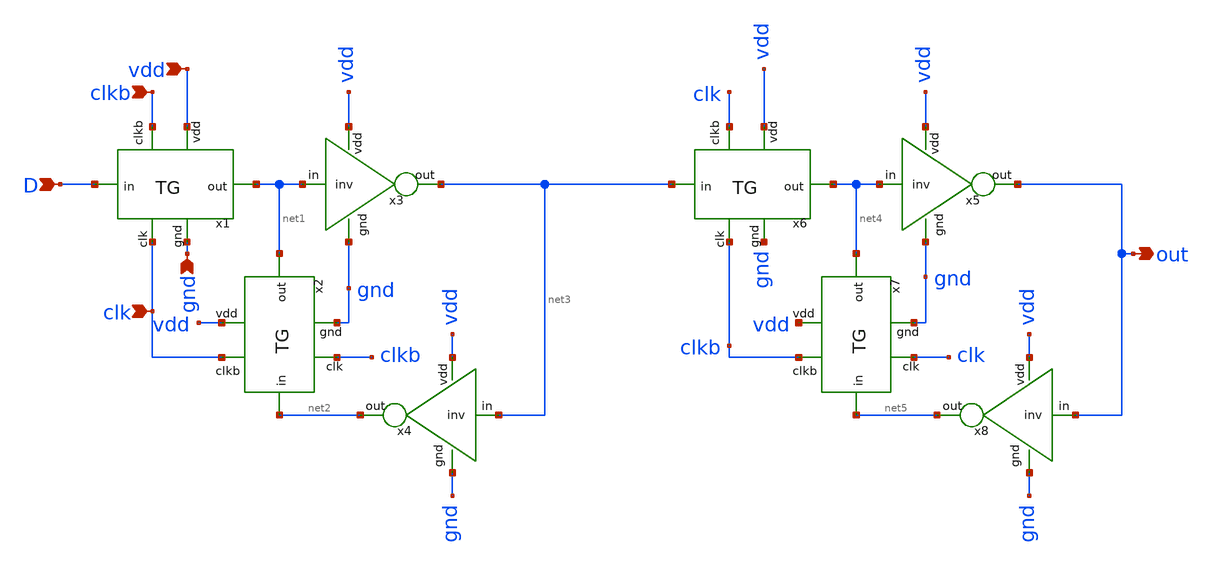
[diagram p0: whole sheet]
** sch_path: pll/dividers_lib/divider_init/xschem/DFF.sch
**.subckt DFF D clk clkb vdd gnd out
*.ipin D
*.ipin clk
*.ipin clkb
*.ipin vdd
*.ipin gnd
*.opin out
x3 vdd net1 net3 gnd inv
x1 clk vdd D net1 gnd clkb TG
x2 clkb vdd net2 net1 gnd clk TG
x4 vdd net3 net2 gnd inv
x5 vdd net4 out gnd inv
x6 clkb vdd net3 net4 gnd clk TG
x7 clk vdd net5 net4 gnd clkb TG
x8 vdd out net5 gnd inv
**.ends
.end
